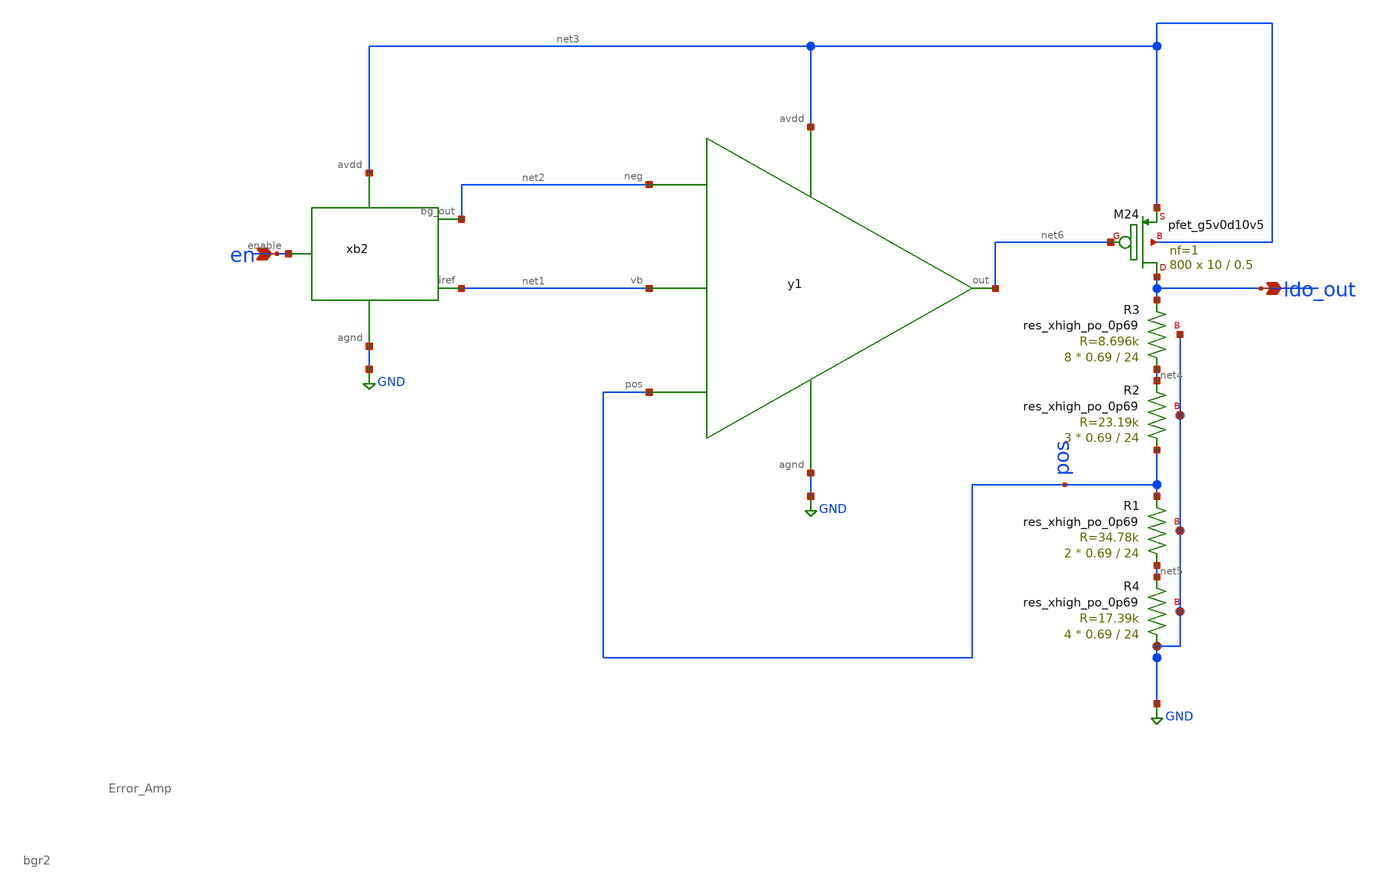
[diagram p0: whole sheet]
** sch_path: xschem/ldo_v2/ldo_v2_lvs.sch
**.subckt ldo_v2_lvs ldo_out en
*.opin ldo_out
*.ipin en
xb2 net2 net1 GND net3 en bgr2
y1 net2 pos net1 net6 net3 GND Error_Amp
XM24 ldo_out net6 net3 net3 sky130_fd_pr__pfet_g5v0d10v5 L=0.5 W=10 nf=1 ad='int((nf+1)/2) * W/nf * 0.29'
+ as='int((nf+2)/2) * W/nf * 0.29' pd='2*int((nf+1)/2) * (W/nf + 0.29)' ps='2*int((nf+2)/2) * (W/nf + 0.29)'
+ nrd='0.29 / W' nrs='0.29 / W' sa=0 sb=0 sd=0 mult=800 m=800
XR2 pos net4 GND sky130_fd_pr__res_xhigh_po_0p69 L=24 mult=3 m=3
XR3 net4 ldo_out GND sky130_fd_pr__res_xhigh_po_0p69 L=24 mult=8 m=8
XR1 net5 pos GND sky130_fd_pr__res_xhigh_po_0p69 L=24 mult=2 m=2
XR4 GND net5 GND sky130_fd_pr__res_xhigh_po_0p69 L=24 mult=4 m=4
**.ends

* expanding   symbol:  ldo_v2/bgr2.sym # of pins=5
** sym_path: xschem/ldo_v2/bgr2.sym
** sch_path: xschem/ldo_v2/bgr2.sch
.subckt bgr2 bg_out iref agnd avdd enable
*.ipin avdd
*.ipin agnd
*.opin bg_out
*.ipin enable
*.ipin iref
XM1 inn mir avdd avdd sky130_fd_pr__pfet_g5v0d10v5 L=2 W=3 nf=1 ad='int((nf+1)/2) * W/nf * 0.29' as='int((nf+2)/2) * W/nf * 0.29'
+ pd='2*int((nf+1)/2) * (W/nf + 0.29)' ps='2*int((nf+2)/2) * (W/nf + 0.29)' nrd='0.29 / W' nrs='0.29 / W'
+ sa=0 sb=0 sd=0 mult=8 m=8
XM2 inp mir avdd avdd sky130_fd_pr__pfet_g5v0d10v5 L=2 W=3 nf=1 ad='int((nf+1)/2) * W/nf * 0.29' as='int((nf+2)/2) * W/nf * 0.29'
+ pd='2*int((nf+1)/2) * (W/nf + 0.29)' ps='2*int((nf+2)/2) * (W/nf + 0.29)' nrd='0.29 / W' nrs='0.29 / W'
+ sa=0 sb=0 sd=0 mult=8 m=8
XM3 bg_out mir avdd avdd sky130_fd_pr__pfet_g5v0d10v5 L=2 W=3 nf=1 ad='int((nf+1)/2) * W/nf * 0.29' as='int((nf+2)/2) * W/nf * 0.29'
+ pd='2*int((nf+1)/2) * (W/nf + 0.29)' ps='2*int((nf+2)/2) * (W/nf + 0.29)' nrd='0.29 / W' nrs='0.29 / W'
+ sa=0 sb=0 sd=0 mult=8 m=8
XQ1 agnd agnd net2 sky130_fd_pr__pnp_05v5_W0p68L0p68 m=1
XQ5 agnd agnd net1 sky130_fd_pr__pnp_05v5_W0p68L0p68 m=1
XQ6 agnd agnd net1 sky130_fd_pr__pnp_05v5_W0p68L0p68 m=1
XQ7 agnd agnd net1 sky130_fd_pr__pnp_05v5_W0p68L0p68 m=1
XQ9 agnd agnd net1 sky130_fd_pr__pnp_05v5_W0p68L0p68 m=1
XQ11 agnd agnd net1 sky130_fd_pr__pnp_05v5_W0p68L0p68 m=1
XQ13 agnd agnd net1 sky130_fd_pr__pnp_05v5_W0p68L0p68 m=1
XQ15 agnd agnd net1 sky130_fd_pr__pnp_05v5_W0p68L0p68 m=1
XQ17 agnd agnd net1 sky130_fd_pr__pnp_05v5_W0p68L0p68 m=1
XM7 net4 net4 avdd avdd sky130_fd_pr__pfet_g5v0d10v5 L=2 W=3 nf=1 ad='int((nf+1)/2) * W/nf * 0.29' as='int((nf+2)/2) * W/nf * 0.29'
+ pd='2*int((nf+1)/2) * (W/nf + 0.29)' ps='2*int((nf+2)/2) * (W/nf + 0.29)' nrd='0.29 / W' nrs='0.29 / W'
+ sa=0 sb=0 sd=0 mult=4 m=4
XM12 net4 inp net3 agnd sky130_fd_pr__nfet_g5v0d10v5 L=1 W=3 nf=1 ad='int((nf+1)/2) * W/nf * 0.29' as='int((nf+2)/2) * W/nf * 0.29'
+ pd='2*int((nf+1)/2) * (W/nf + 0.29)' ps='2*int((nf+2)/2) * (W/nf + 0.29)' nrd='0.29 / W' nrs='0.29 / W'
+ sa=0 sb=0 sd=0 mult=8 m=8
XM21 mir inn net3 agnd sky130_fd_pr__nfet_g5v0d10v5 L=1 W=3 nf=1 ad='int((nf+1)/2) * W/nf * 0.29' as='int((nf+2)/2) * W/nf * 0.29'
+ pd='2*int((nf+1)/2) * (W/nf + 0.29)' ps='2*int((nf+2)/2) * (W/nf + 0.29)' nrd='0.29 / W' nrs='0.29 / W'
+ sa=0 sb=0 sd=0 mult=8 m=8
XM23 mir net4 avdd avdd sky130_fd_pr__pfet_g5v0d10v5 L=2 W=3 nf=1 ad='int((nf+1)/2) * W/nf * 0.29' as='int((nf+2)/2) * W/nf * 0.29'
+ pd='2*int((nf+1)/2) * (W/nf + 0.29)' ps='2*int((nf+2)/2) * (W/nf + 0.29)' nrd='0.29 / W' nrs='0.29 / W'
+ sa=0 sb=0 sd=0 mult=4 m=4
XM15 net3 net5 agnd agnd sky130_fd_pr__nfet_g5v0d10v5 L=2 W=5 nf=1 ad='int((nf+1)/2) * W/nf * 0.29' as='int((nf+2)/2) * W/nf * 0.29'
+ pd='2*int((nf+1)/2) * (W/nf + 0.29)' ps='2*int((nf+2)/2) * (W/nf + 0.29)' nrd='0.29 / W' nrs='0.29 / W'
+ sa=0 sb=0 sd=0 mult=4 m=4
XM25 net5 mir avdd avdd sky130_fd_pr__pfet_g5v0d10v5 L=2 W=3 nf=1 ad='int((nf+1)/2) * W/nf * 0.29' as='int((nf+2)/2) * W/nf * 0.29'
+ pd='2*int((nf+1)/2) * (W/nf + 0.29)' ps='2*int((nf+2)/2) * (W/nf + 0.29)' nrd='0.29 / W' nrs='0.29 / W'
+ sa=0 sb=0 sd=0 mult=8 m=8
XM16 net5 net5 agnd agnd sky130_fd_pr__nfet_g5v0d10v5 L=2 W=5 nf=1 ad='int((nf+1)/2) * W/nf * 0.29' as='int((nf+2)/2) * W/nf * 0.29'
+ pd='2*int((nf+1)/2) * (W/nf + 0.29)' ps='2*int((nf+2)/2) * (W/nf + 0.29)' nrd='0.29 / W' nrs='0.29 / W'
+ sa=0 sb=0 sd=0 mult=4 m=4
XC1 mir agnd sky130_fd_pr__cap_mim_m3_1 W=16 L=16 MF=1 m=1
XR1 net6 inp agnd sky130_fd_pr__res_xhigh_po_0p69 L=27 mult=3 m=3
XR2 net2 inn agnd sky130_fd_pr__res_xhigh_po_0p69 L=27 mult=3 m=3
XR3 net8 net2 agnd sky130_fd_pr__res_xhigh_po_0p69 L=27 mult=1 m=1
XR10 net1 net6 agnd sky130_fd_pr__res_xhigh_po_0p69 L=27 mult=6 m=6
XR4 agnd net7 agnd sky130_fd_pr__res_xhigh_po_0p69 L=27 mult=15 m=15
XR11 agnd net8 agnd sky130_fd_pr__res_xhigh_po_0p69 L=27 mult=15 m=15
XR6 net7 net6 agnd sky130_fd_pr__res_xhigh_po_0p69 L=27 mult=1 m=1
XR5 net9 bg_out agnd sky130_fd_pr__res_xhigh_po_0p69 L=27 mult=1 m=1
XR14 agnd net9 agnd sky130_fd_pr__res_xhigh_po_0p69 L=27 mult=53 m=53
XM19 mir enable avdd avdd sky130_fd_pr__pfet_g5v0d10v5 L=0.5 W=0.42 nf=1 ad='int((nf+1)/2) * W/nf * 0.29'
+ as='int((nf+2)/2) * W/nf * 0.29' pd='2*int((nf+1)/2) * (W/nf + 0.29)' ps='2*int((nf+2)/2) * (W/nf + 0.29)'
+ nrd='0.29 / W' nrs='0.29 / W' sa=0 sb=0 sd=0 mult=2 m=2
XM4 net10 bg_out avdd avdd sky130_fd_pr__pfet_g5v0d10v5 L=5 W=0.42 nf=1 ad='int((nf+1)/2) * W/nf * 0.29'
+ as='int((nf+2)/2) * W/nf * 0.29' pd='2*int((nf+1)/2) * (W/nf + 0.29)' ps='2*int((nf+2)/2) * (W/nf + 0.29)'
+ nrd='0.29 / W' nrs='0.29 / W' sa=0 sb=0 sd=0 mult=2 m=2
XM5 net10 bg_out agnd agnd sky130_fd_pr__nfet_g5v0d10v5 L=0.5 W=10 nf=1 ad='int((nf+1)/2) * W/nf * 0.29'
+ as='int((nf+2)/2) * W/nf * 0.29' pd='2*int((nf+1)/2) * (W/nf + 0.29)' ps='2*int((nf+2)/2) * (W/nf + 0.29)'
+ nrd='0.29 / W' nrs='0.29 / W' sa=0 sb=0 sd=0 mult=8 m=8
XM6 avdd net10 inn agnd sky130_fd_pr__nfet_g5v0d10v5 L=0.5 W=3 nf=1 ad='int((nf+1)/2) * W/nf * 0.29'
+ as='int((nf+2)/2) * W/nf * 0.29' pd='2*int((nf+1)/2) * (W/nf + 0.29)' ps='2*int((nf+2)/2) * (W/nf + 0.29)'
+ nrd='0.29 / W' nrs='0.29 / W' sa=0 sb=0 sd=0 mult=4 m=4
XM26 iref mir avdd avdd sky130_fd_pr__pfet_g5v0d10v5 L=2 W=3 nf=1 ad='int((nf+1)/2) * W/nf * 0.29' as='int((nf+2)/2) * W/nf * 0.29'
+ pd='2*int((nf+1)/2) * (W/nf + 0.29)' ps='2*int((nf+2)/2) * (W/nf + 0.29)' nrd='0.29 / W' nrs='0.29 / W'
+ sa=0 sb=0 sd=0 mult=4 m=4
.ends


* expanding   symbol:  ldo_v1/Error_Amp.sym # of pins=6
** sym_path: xschem/ldo_v1/Error_Amp.sym
** sch_path: xschem/ldo_v1/Error_Amp.sch
.subckt Error_Amp neg pos vb out avdd agnd
*.opin out
*.iopin avdd
*.iopin agnd
*.iopin vb
*.ipin neg
*.ipin pos
XM8 net2 net2 avdd avdd sky130_fd_pr__pfet_g5v0d10v5 L=1.2 W=3 nf=1 ad='int((nf+1)/2) * W/nf * 0.29'
+ as='int((nf+2)/2) * W/nf * 0.29' pd='2*int((nf+1)/2) * (W/nf + 0.29)' ps='2*int((nf+2)/2) * (W/nf + 0.29)'
+ nrd='0.29 / W' nrs='0.29 / W' sa=0 sb=0 sd=0 mult=4 m=4
XM9 net2 neg net3 agnd sky130_fd_pr__nfet_g5v0d10v5 L=1 W=2 nf=1 ad='int((nf+1)/2) * W/nf * 0.29' as='int((nf+2)/2) * W/nf * 0.29'
+ pd='2*int((nf+1)/2) * (W/nf + 0.29)' ps='2*int((nf+2)/2) * (W/nf + 0.29)' nrd='0.29 / W' nrs='0.29 / W'
+ sa=0 sb=0 sd=0 mult=8 m=8
XM10 net1 pos net3 agnd sky130_fd_pr__nfet_g5v0d10v5 L=1 W=2 nf=1 ad='int((nf+1)/2) * W/nf * 0.29' as='int((nf+2)/2) * W/nf * 0.29'
+ pd='2*int((nf+1)/2) * (W/nf + 0.29)' ps='2*int((nf+2)/2) * (W/nf + 0.29)' nrd='0.29 / W' nrs='0.29 / W'
+ sa=0 sb=0 sd=0 mult=8 m=8
XM11 net1 net2 avdd avdd sky130_fd_pr__pfet_g5v0d10v5 L=1.2 W=3 nf=1 ad='int((nf+1)/2) * W/nf * 0.29'
+ as='int((nf+2)/2) * W/nf * 0.29' pd='2*int((nf+1)/2) * (W/nf + 0.29)' ps='2*int((nf+2)/2) * (W/nf + 0.29)'
+ nrd='0.29 / W' nrs='0.29 / W' sa=0 sb=0 sd=0 mult=4 m=4
XM13 net3 vb agnd agnd sky130_fd_pr__nfet_g5v0d10v5 L=1 W=1 nf=1 ad='int((nf+1)/2) * W/nf * 0.29' as='int((nf+2)/2) * W/nf * 0.29'
+ pd='2*int((nf+1)/2) * (W/nf + 0.29)' ps='2*int((nf+2)/2) * (W/nf + 0.29)' nrd='0.29 / W' nrs='0.29 / W'
+ sa=0 sb=0 sd=0 mult=8 m=8
XM14 out net1 avdd avdd sky130_fd_pr__pfet_g5v0d10v5 L=1.2 W=3 nf=1 ad='int((nf+1)/2) * W/nf * 0.29'
+ as='int((nf+2)/2) * W/nf * 0.29' pd='2*int((nf+1)/2) * (W/nf + 0.29)' ps='2*int((nf+2)/2) * (W/nf + 0.29)'
+ nrd='0.29 / W' nrs='0.29 / W' sa=0 sb=0 sd=0 mult=12 m=12
XM18 out vb agnd agnd sky130_fd_pr__nfet_g5v0d10v5 L=1 W=1 nf=1 ad='int((nf+1)/2) * W/nf * 0.29' as='int((nf+2)/2) * W/nf * 0.29'
+ pd='2*int((nf+1)/2) * (W/nf + 0.29)' ps='2*int((nf+2)/2) * (W/nf + 0.29)' nrd='0.29 / W' nrs='0.29 / W'
+ sa=0 sb=0 sd=0 mult=12 m=12
XC3 net1 net4 sky130_fd_pr__cap_mim_m3_1 W=50 L=50 MF=1 m=1
XR7 out net4 agnd sky130_fd_pr__res_xhigh_po_0p69 L=4.5 mult=1 m=1
XM20 vb vb agnd agnd sky130_fd_pr__nfet_g5v0d10v5 L=1 W=1 nf=1 ad='int((nf+1)/2) * W/nf * 0.29' as='int((nf+2)/2) * W/nf * 0.29'
+ pd='2*int((nf+1)/2) * (W/nf + 0.29)' ps='2*int((nf+2)/2) * (W/nf + 0.29)' nrd='0.29 / W' nrs='0.29 / W'
+ sa=0 sb=0 sd=0 mult=4 m=4
.ends

.GLOBAL GND
.end
